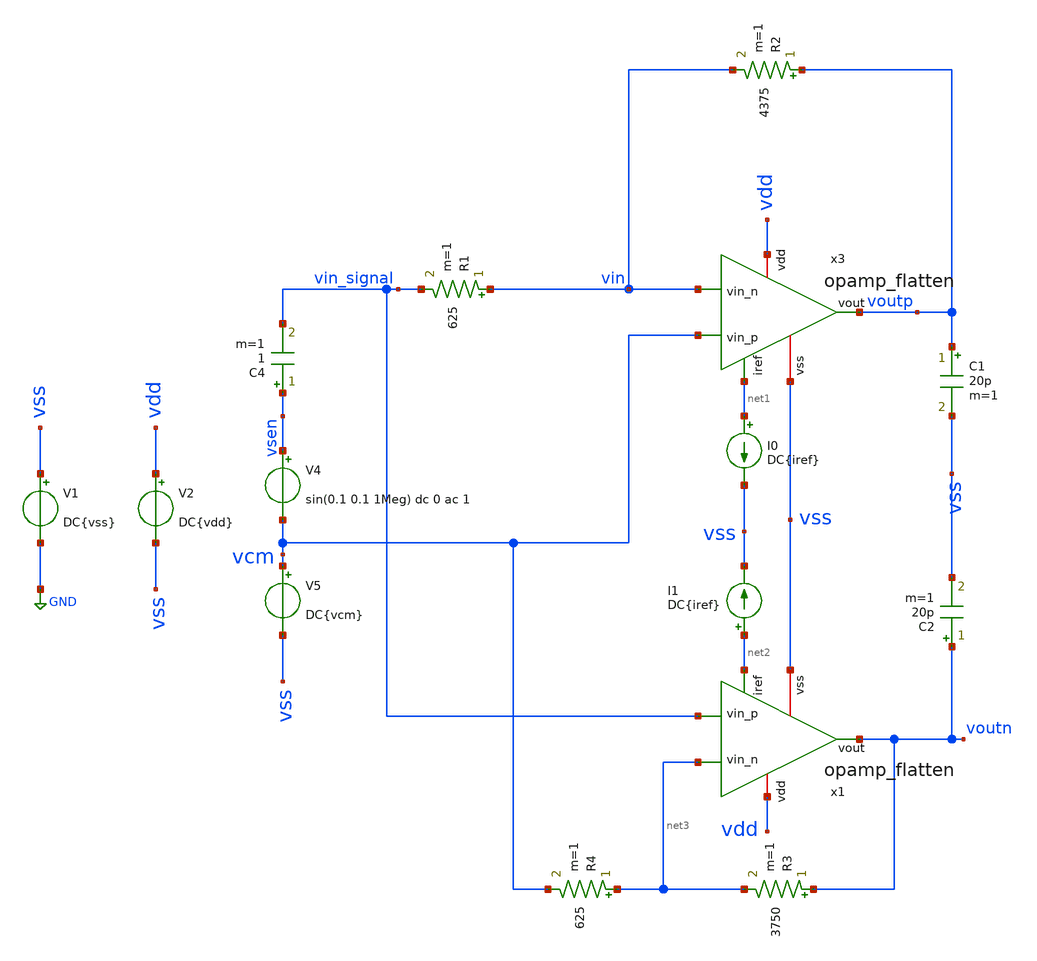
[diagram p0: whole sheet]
** sch_path: sch/two_opamps_postLay.sch
**.subckt two_opamps_postLay
V1 vss GND DC{vss}
V2 vdd vss DC{vdd}
V4 vsen vcm sin(0.1 0.1 1Meg) dc 0 ac 1
C4 vsen vin_signal 1 m=1
I0 net1 vss DC{iref}
R1 vin vin_signal 625 m=1
C1 voutp vss 20p m=1
V5 vcm vss DC{vcm}
R2 voutp vin 4375 m=1
I1 net2 vss DC{iref}
R3 voutn net3 3750 m=1
R4 net3 vcm 625 m=1
C2 voutn vss 20p m=1
x3 vdd net1 vin vcm voutp vss opamp_flatten
x1 vdd net2 net3 vin_signal voutn vss opamp_flatten
**** begin user architecture code




* Circuit Parameters
.param iref = 100u
.param vdd  = 1.8
.param vss  = 0.0
.param vcm  = 0.7
.options TEMP = 65.0

* Include Models
*.lib ~/skywater_pdk/skywater-pdk/libraries/sky130_fd_pr/latest/models/corners/sky130.lib TT

* OP Parameters & Singals to save
.save all

*Simulations
.control


  reset
  tran 0.01u 11u
  setplot tran1
  plot v(vsen) v(vcm) v(voutp) v(voutn)
  plot i(v4)

  write ~/Desktop/EDA/TIA_IPN/sch/sim_results/two_opamps_postLay.raw



.endc

.end



** opencircuitdesign pdks install
.lib $::SKYWATER_MODELS/sky130.lib.spice tt
.inc /home/alex/Desktop/EDA/TIA_IPN/mag/opamp_flatten.spice

**** end user architecture code
**.ends
.GLOBAL GND
.end
